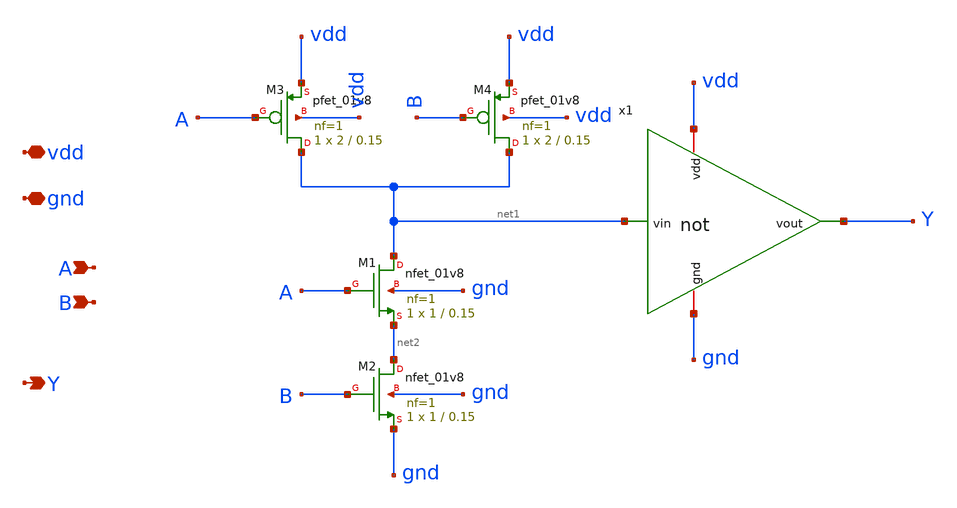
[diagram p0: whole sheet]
** sch_path: LogicGates/and.sch
**.subckt and A B vdd gnd Y
*.ipin A
*.ipin B
*.iopin vdd
*.iopin gnd
*.opin Y
XM1 net1 A net2 gnd sky130_fd_pr__nfet_01v8 L=0.15 W=1 nf=1 ad='int((nf+1)/2) * W/nf * 0.29' as='int((nf+2)/2) * W/nf * 0.29'
+ pd='2*int((nf+1)/2) * (W/nf + 0.29)' ps='2*int((nf+2)/2) * (W/nf + 0.29)' nrd='0.29 / W' nrs='0.29 / W'
+ sa=0 sb=0 sd=0 mult=1 m=1
XM2 net2 B gnd gnd sky130_fd_pr__nfet_01v8 L=0.15 W=1 nf=1 ad='int((nf+1)/2) * W/nf * 0.29' as='int((nf+2)/2) * W/nf * 0.29'
+ pd='2*int((nf+1)/2) * (W/nf + 0.29)' ps='2*int((nf+2)/2) * (W/nf + 0.29)' nrd='0.29 / W' nrs='0.29 / W'
+ sa=0 sb=0 sd=0 mult=1 m=1
XM3 net1 A vdd vdd sky130_fd_pr__pfet_01v8 L=0.15 W=2 nf=1 ad='int((nf+1)/2) * W/nf * 0.29' as='int((nf+2)/2) * W/nf * 0.29'
+ pd='2*int((nf+1)/2) * (W/nf + 0.29)' ps='2*int((nf+2)/2) * (W/nf + 0.29)' nrd='0.29 / W' nrs='0.29 / W'
+ sa=0 sb=0 sd=0 mult=1 m=1
XM4 net1 B vdd vdd sky130_fd_pr__pfet_01v8 L=0.15 W=2 nf=1 ad='int((nf+1)/2) * W/nf * 0.29' as='int((nf+2)/2) * W/nf * 0.29'
+ pd='2*int((nf+1)/2) * (W/nf + 0.29)' ps='2*int((nf+2)/2) * (W/nf + 0.29)' nrd='0.29 / W' nrs='0.29 / W'
+ sa=0 sb=0 sd=0 mult=1 m=1
x1 vdd gnd net1 Y not
**.ends

* expanding   symbol:  LogicGates/not.sym # of pins=4
** sym_path: LogicGates/not.sym
** sch_path: LogicGates/not.sch
.subckt not vdd gnd vin vout
*.ipin vin
*.iopin vdd
*.iopin gnd
*.opin vout
XM2 vout vin vdd vdd sky130_fd_pr__pfet_01v8 L=0.15 W=2 nf=1 ad='int((nf+1)/2) * W/nf * 0.29' as='int((nf+2)/2) * W/nf * 0.29'
+ pd='2*int((nf+1)/2) * (W/nf + 0.29)' ps='2*int((nf+2)/2) * (W/nf + 0.29)' nrd='0.29 / W' nrs='0.29 / W'
+ sa=0 sb=0 sd=0 mult=1 m=1
XM1 vout vin gnd gnd sky130_fd_pr__nfet_01v8 L=0.15 W=1 nf=1 ad='int((nf+1)/2) * W/nf * 0.29' as='int((nf+2)/2) * W/nf * 0.29'
+ pd='2*int((nf+1)/2) * (W/nf + 0.29)' ps='2*int((nf+2)/2) * (W/nf + 0.29)' nrd='0.29 / W' nrs='0.29 / W'
+ sa=0 sb=0 sd=0 mult=1 m=1
.ends

.end
